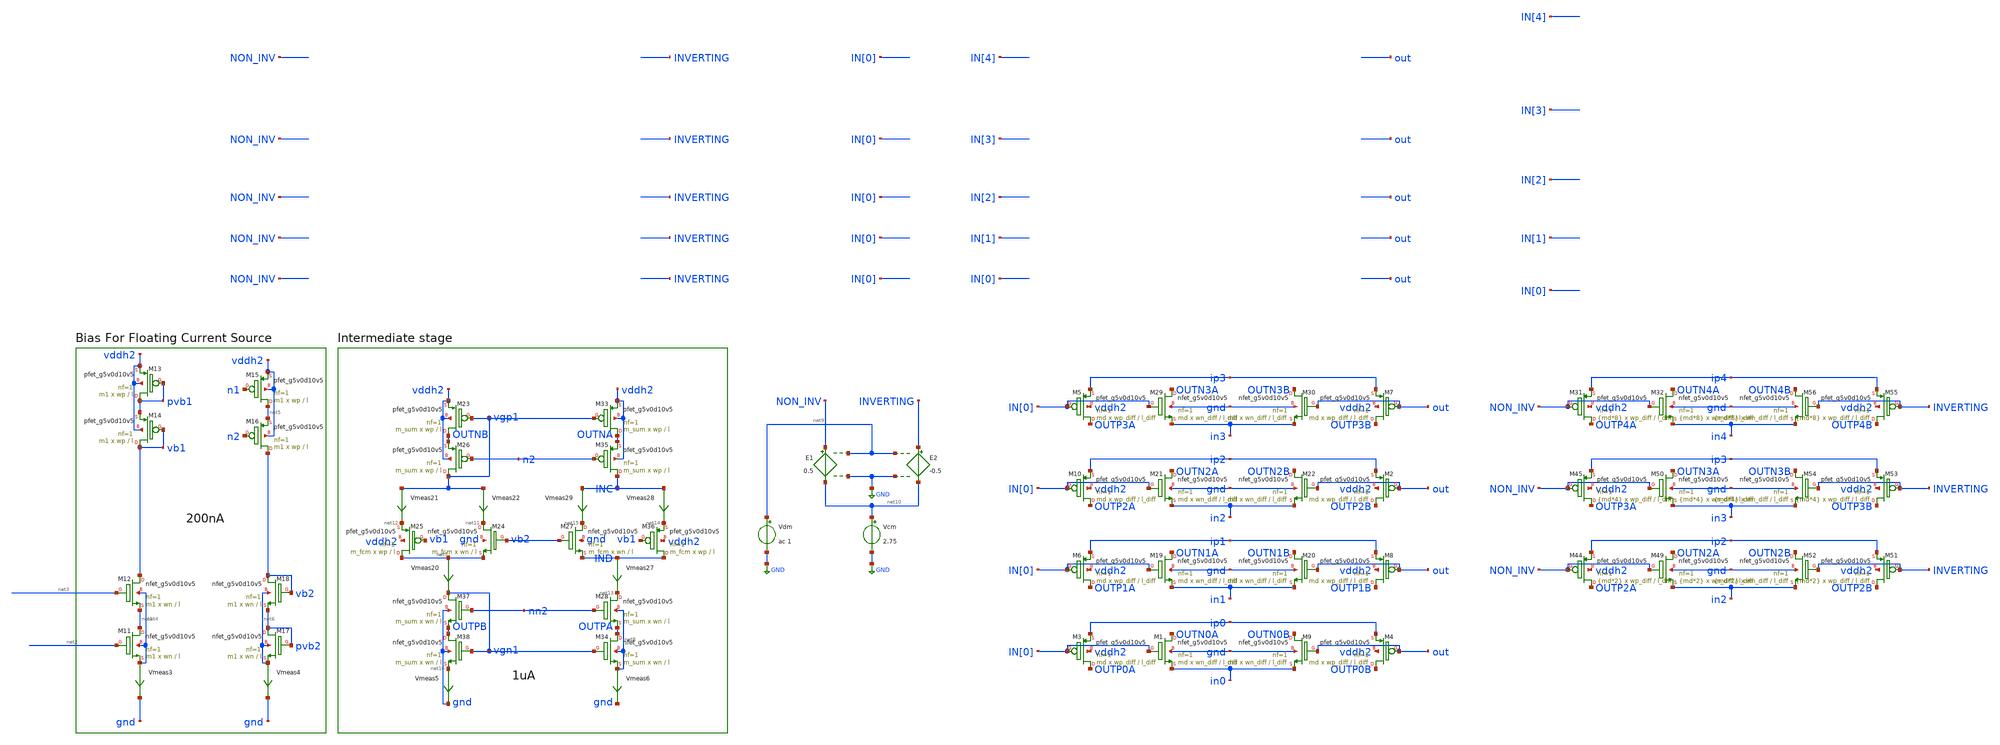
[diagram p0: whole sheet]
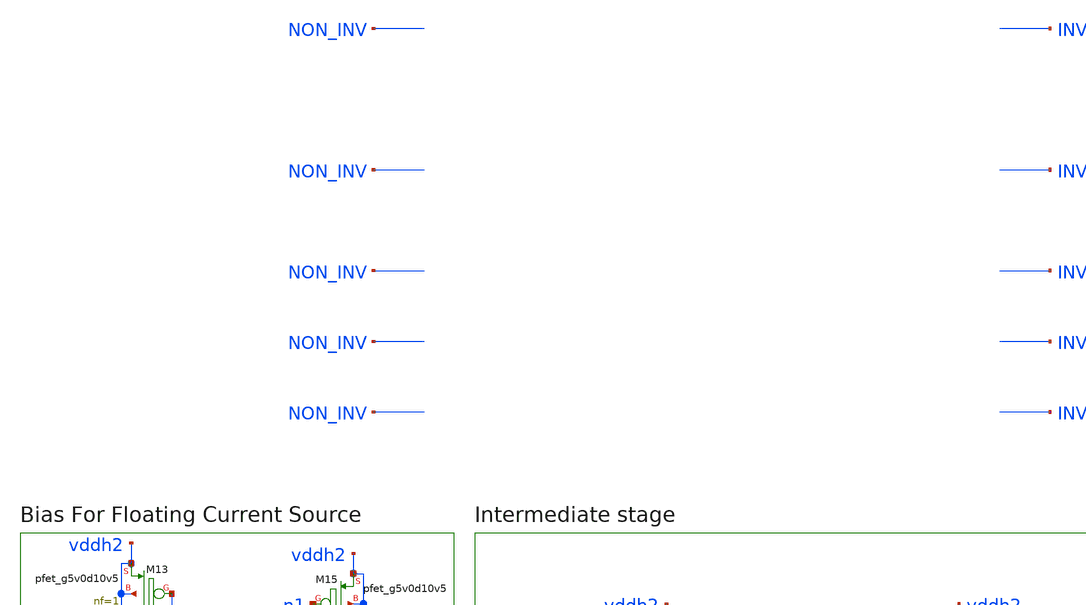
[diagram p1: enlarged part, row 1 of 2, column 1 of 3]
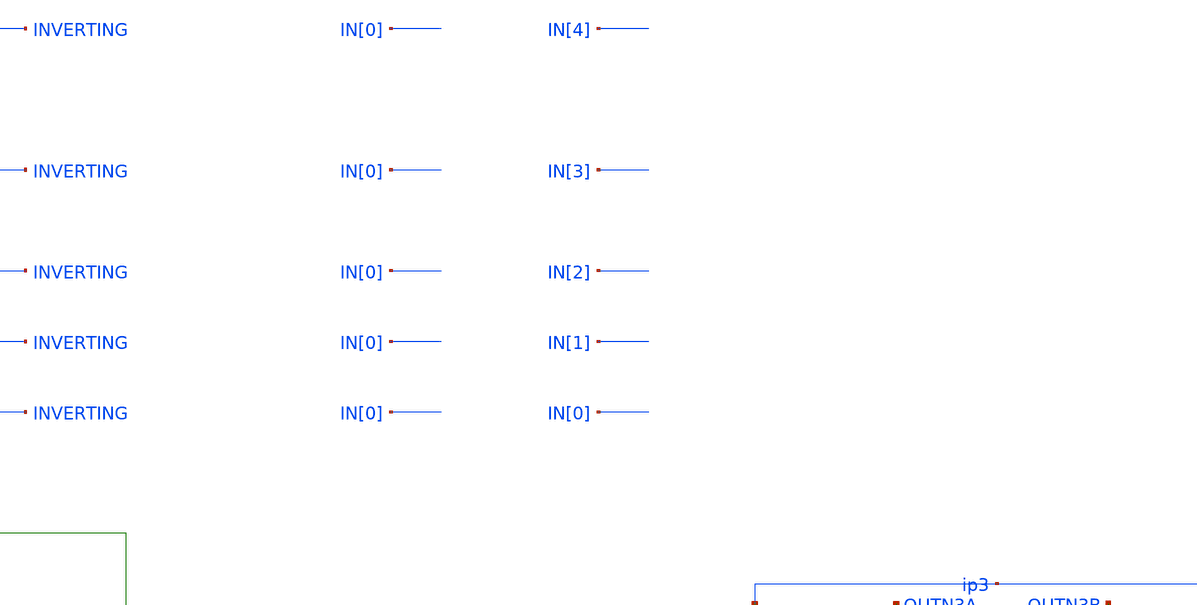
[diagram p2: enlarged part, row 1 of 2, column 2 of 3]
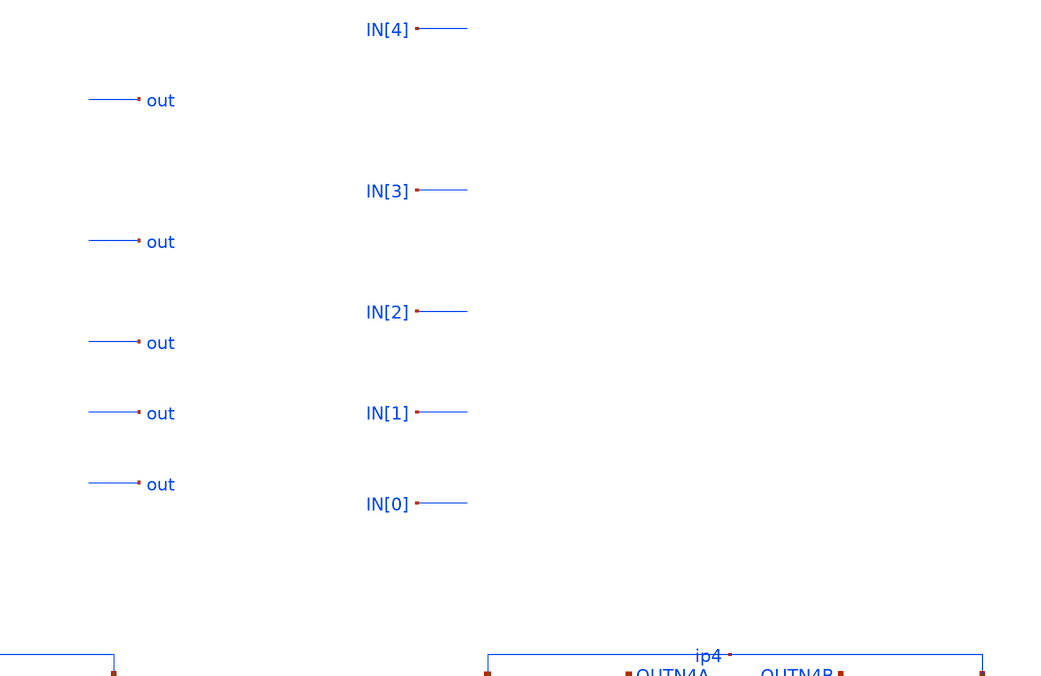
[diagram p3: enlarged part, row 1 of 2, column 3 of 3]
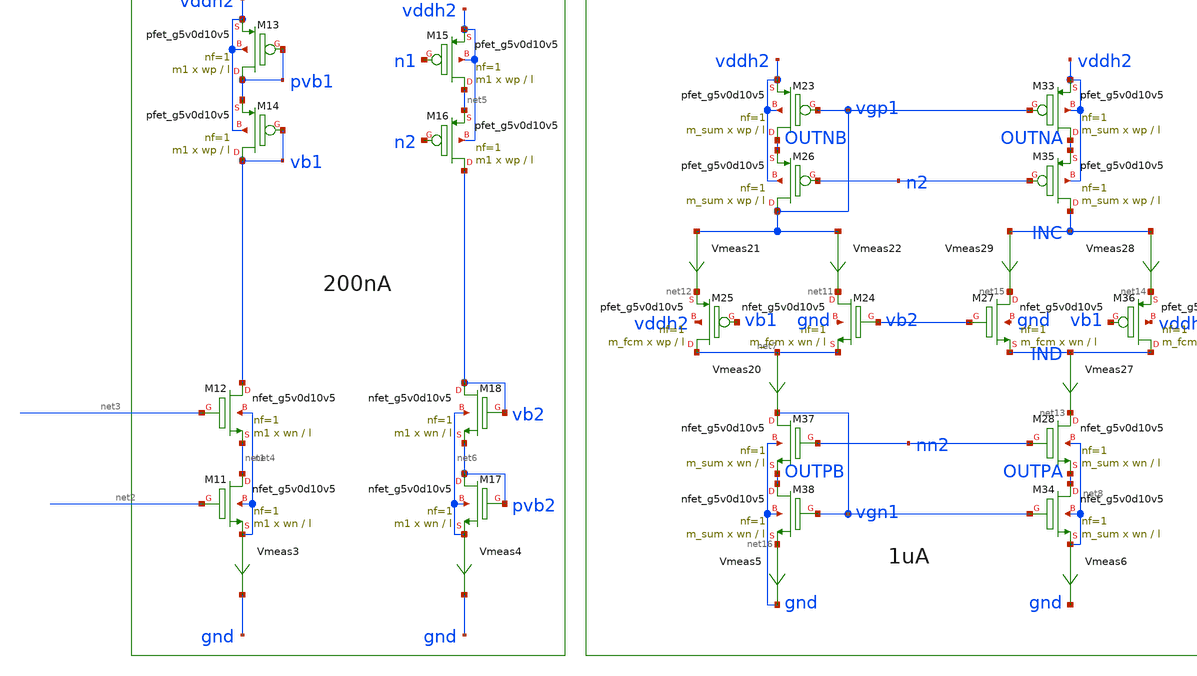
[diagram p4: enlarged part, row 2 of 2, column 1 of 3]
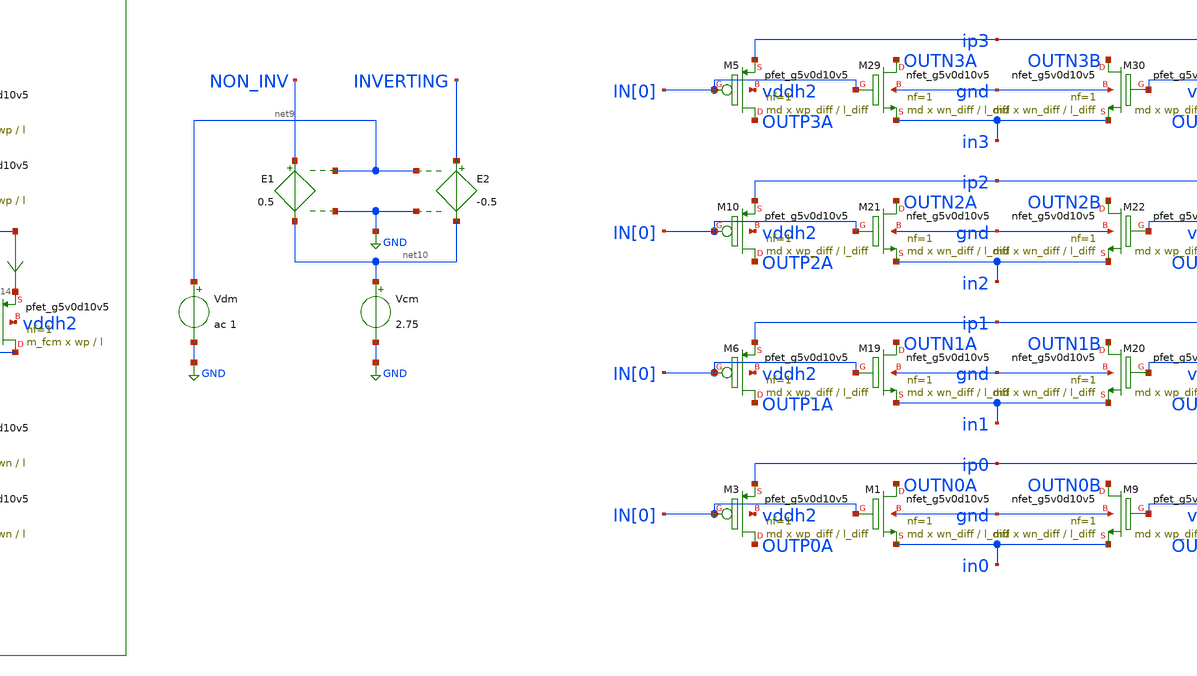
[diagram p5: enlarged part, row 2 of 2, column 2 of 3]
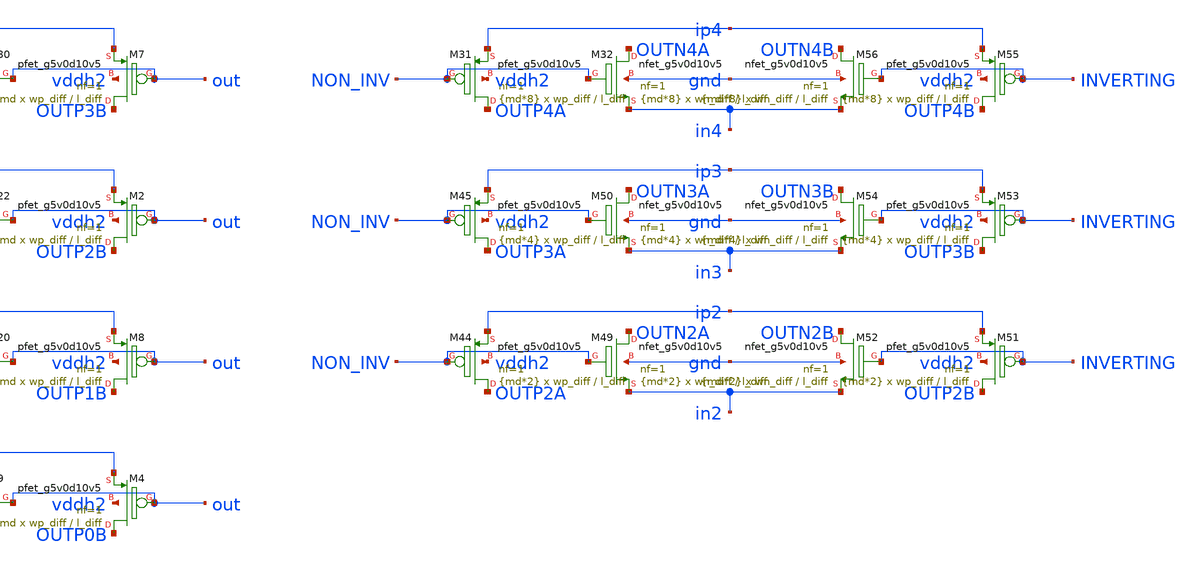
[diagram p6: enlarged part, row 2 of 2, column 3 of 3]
** sch_path: xschem/untitled-1.sch
**.subckt untitled-1
XM11 net1 net2 net4 net4 sky130_fd_pr__nfet_g5v0d10v5 L=l W=wn nf=1 ad='int((nf+1)/2) * W/nf * 0.29'
+ as='int((nf+2)/2) * W/nf * 0.29' pd='2*int((nf+1)/2) * (W/nf + 0.29)' ps='2*int((nf+2)/2) * (W/nf + 0.29)'
+ nrd='0.29 / W' nrs='0.29 / W' sa=0 sb=0 sd=0 mult=m1 m=m1
XM12 vb1 net3 net1 net4 sky130_fd_pr__nfet_g5v0d10v5 L=l W=wn nf=1 ad='int((nf+1)/2) * W/nf * 0.29' as='int((nf+2)/2) * W/nf * 0.29'
+ pd='2*int((nf+1)/2) * (W/nf + 0.29)' ps='2*int((nf+2)/2) * (W/nf + 0.29)' nrd='0.29 / W' nrs='0.29 / W'
+ sa=0 sb=0 sd=0 mult=m1 m=m1
Vmeas3 net4 gnd 0
.save i(vmeas3)
XM17 pvb2 pvb2 net6 net6 sky130_fd_pr__nfet_g5v0d10v5 L=l W=wn nf=1 ad='int((nf+1)/2) * W/nf * 0.29'
+ as='int((nf+2)/2) * W/nf * 0.29' pd='2*int((nf+1)/2) * (W/nf + 0.29)' ps='2*int((nf+2)/2) * (W/nf + 0.29)'
+ nrd='0.29 / W' nrs='0.29 / W' sa=0 sb=0 sd=0 mult=m1 m=m1
XM18 vb2 vb2 pvb2 net6 sky130_fd_pr__nfet_g5v0d10v5 L=l W=wn nf=1 ad='int((nf+1)/2) * W/nf * 0.29' as='int((nf+2)/2) * W/nf * 0.29'
+ pd='2*int((nf+1)/2) * (W/nf + 0.29)' ps='2*int((nf+2)/2) * (W/nf + 0.29)' nrd='0.29 / W' nrs='0.29 / W'
+ sa=0 sb=0 sd=0 mult=m1 m=m1
Vmeas4 net6 gnd 0
.save i(vmeas4)
Vmeas20 net7 vgn1 0
.save i(vmeas20)
XM23 OUTNB vgp1 vddh2 vddh2 sky130_fd_pr__pfet_g5v0d10v5 L=l W=wp nf=1 ad='int((nf+1)/2) * W/nf * 0.29'
+ as='int((nf+2)/2) * W/nf * 0.29' pd='2*int((nf+1)/2) * (W/nf + 0.29)' ps='2*int((nf+2)/2) * (W/nf + 0.29)'
+ nrd='0.29 / W' nrs='0.29 / W' sa=0 sb=0 sd=0 mult=m_sum m=m_sum
XM24 net11 vb2 net7 gnd sky130_fd_pr__nfet_g5v0d10v5 L=l W=wn nf=1 ad='int((nf+1)/2) * W/nf * 0.29' as='int((nf+2)/2) * W/nf * 0.29'
+ pd='2*int((nf+1)/2) * (W/nf + 0.29)' ps='2*int((nf+2)/2) * (W/nf + 0.29)' nrd='0.29 / W' nrs='0.29 / W'
+ sa=0 sb=0 sd=0 mult=m_fcm m=m_fcm
Vmeas21 vgp1 net12 0
.save i(vmeas21)
Vmeas22 vgp1 net11 0
.save i(vmeas22)
XM25 net7 vb1 net12 vddh2 sky130_fd_pr__pfet_g5v0d10v5 L=l W=wp nf=1 ad='int((nf+1)/2) * W/nf * 0.29'
+ as='int((nf+2)/2) * W/nf * 0.29' pd='2*int((nf+1)/2) * (W/nf + 0.29)' ps='2*int((nf+2)/2) * (W/nf + 0.29)'
+ nrd='0.29 / W' nrs='0.29 / W' sa=0 sb=0 sd=0 mult=m_fcm m=m_fcm
Vmeas27 IND net13 0
.save i(vmeas27)
Vmeas28 INC net14 0
.save i(vmeas28)
Vmeas29 INC net15 0
.save i(vmeas29)
XM26 vgp1 n2 OUTNB vddh2 sky130_fd_pr__pfet_g5v0d10v5 L=l W=wp nf=1 ad='int((nf+1)/2) * W/nf * 0.29'
+ as='int((nf+2)/2) * W/nf * 0.29' pd='2*int((nf+1)/2) * (W/nf + 0.29)' ps='2*int((nf+2)/2) * (W/nf + 0.29)'
+ nrd='0.29 / W' nrs='0.29 / W' sa=0 sb=0 sd=0 mult=m_sum m=m_sum
XM33 OUTNA vgp1 vddh2 vddh2 sky130_fd_pr__pfet_g5v0d10v5 L=l W=wp nf=1 ad='int((nf+1)/2) * W/nf * 0.29'
+ as='int((nf+2)/2) * W/nf * 0.29' pd='2*int((nf+1)/2) * (W/nf + 0.29)' ps='2*int((nf+2)/2) * (W/nf + 0.29)'
+ nrd='0.29 / W' nrs='0.29 / W' sa=0 sb=0 sd=0 mult=m_sum m=m_sum
XM35 INC n2 OUTNA vddh2 sky130_fd_pr__pfet_g5v0d10v5 L=l W=wp nf=1 ad='int((nf+1)/2) * W/nf * 0.29' as='int((nf+2)/2) * W/nf * 0.29'
+ pd='2*int((nf+1)/2) * (W/nf + 0.29)' ps='2*int((nf+2)/2) * (W/nf + 0.29)' nrd='0.29 / W' nrs='0.29 / W'
+ sa=0 sb=0 sd=0 mult=m_sum m=m_sum
XM28 net13 nn2 OUTPA net8 sky130_fd_pr__nfet_g5v0d10v5 L=l W=wn nf=1 ad='int((nf+1)/2) * W/nf * 0.29'
+ as='int((nf+2)/2) * W/nf * 0.29' pd='2*int((nf+1)/2) * (W/nf + 0.29)' ps='2*int((nf+2)/2) * (W/nf + 0.29)'
+ nrd='0.29 / W' nrs='0.29 / W' sa=0 sb=0 sd=0 mult=m_sum m=m_sum
XM34 OUTPA vgn1 net8 net8 sky130_fd_pr__nfet_g5v0d10v5 L=l W=wn nf=1 ad='int((nf+1)/2) * W/nf * 0.29'
+ as='int((nf+2)/2) * W/nf * 0.29' pd='2*int((nf+1)/2) * (W/nf + 0.29)' ps='2*int((nf+2)/2) * (W/nf + 0.29)'
+ nrd='0.29 / W' nrs='0.29 / W' sa=0 sb=0 sd=0 mult=m_sum m=m_sum
XM37 vgn1 nn2 OUTPB gnd sky130_fd_pr__nfet_g5v0d10v5 L=l W=wn nf=1 ad='int((nf+1)/2) * W/nf * 0.29' as='int((nf+2)/2) * W/nf * 0.29'
+ pd='2*int((nf+1)/2) * (W/nf + 0.29)' ps='2*int((nf+2)/2) * (W/nf + 0.29)' nrd='0.29 / W' nrs='0.29 / W'
+ sa=0 sb=0 sd=0 mult=m_sum m=m_sum
XM38 OUTPB vgn1 net16 gnd sky130_fd_pr__nfet_g5v0d10v5 L=l W=wn nf=1 ad='int((nf+1)/2) * W/nf * 0.29'
+ as='int((nf+2)/2) * W/nf * 0.29' pd='2*int((nf+1)/2) * (W/nf + 0.29)' ps='2*int((nf+2)/2) * (W/nf + 0.29)'
+ nrd='0.29 / W' nrs='0.29 / W' sa=0 sb=0 sd=0 mult=m_sum m=m_sum
XM36 IND vb1 net14 vddh2 sky130_fd_pr__pfet_g5v0d10v5 L=l W=wp nf=1 ad='int((nf+1)/2) * W/nf * 0.29'
+ as='int((nf+2)/2) * W/nf * 0.29' pd='2*int((nf+1)/2) * (W/nf + 0.29)' ps='2*int((nf+2)/2) * (W/nf + 0.29)'
+ nrd='0.29 / W' nrs='0.29 / W' sa=0 sb=0 sd=0 mult=m_fcm m=m_fcm
XM27 net15 vb2 IND gnd sky130_fd_pr__nfet_g5v0d10v5 L=l W=wn nf=1 ad='int((nf+1)/2) * W/nf * 0.29' as='int((nf+2)/2) * W/nf * 0.29'
+ pd='2*int((nf+1)/2) * (W/nf + 0.29)' ps='2*int((nf+2)/2) * (W/nf + 0.29)' nrd='0.29 / W' nrs='0.29 / W'
+ sa=0 sb=0 sd=0 mult=m_fcm m=m_fcm
XM13 pvb1 pvb1 vddh2 vddh2 sky130_fd_pr__pfet_g5v0d10v5 L=l W=wp nf=1 ad='int((nf+1)/2) * W/nf * 0.29'
+ as='int((nf+2)/2) * W/nf * 0.29' pd='2*int((nf+1)/2) * (W/nf + 0.29)' ps='2*int((nf+2)/2) * (W/nf + 0.29)'
+ nrd='0.29 / W' nrs='0.29 / W' sa=0 sb=0 sd=0 mult=m1 m=m1
XM14 vb1 vb1 pvb1 vddh2 sky130_fd_pr__pfet_g5v0d10v5 L=l W=wp nf=1 ad='int((nf+1)/2) * W/nf * 0.29' as='int((nf+2)/2) * W/nf * 0.29'
+ pd='2*int((nf+1)/2) * (W/nf + 0.29)' ps='2*int((nf+2)/2) * (W/nf + 0.29)' nrd='0.29 / W' nrs='0.29 / W'
+ sa=0 sb=0 sd=0 mult=m1 m=m1
XM15 net5 n1 vddh2 vddh2 sky130_fd_pr__pfet_g5v0d10v5 L=l W=wp nf=1 ad='int((nf+1)/2) * W/nf * 0.29'
+ as='int((nf+2)/2) * W/nf * 0.29' pd='2*int((nf+1)/2) * (W/nf + 0.29)' ps='2*int((nf+2)/2) * (W/nf + 0.29)'
+ nrd='0.29 / W' nrs='0.29 / W' sa=0 sb=0 sd=0 mult=m1 m=m1
XM16 vb2 n2 net5 vddh2 sky130_fd_pr__pfet_g5v0d10v5 L=l W=wp nf=1 ad='int((nf+1)/2) * W/nf * 0.29' as='int((nf+2)/2) * W/nf * 0.29'
+ pd='2*int((nf+1)/2) * (W/nf + 0.29)' ps='2*int((nf+2)/2) * (W/nf + 0.29)' nrd='0.29 / W' nrs='0.29 / W'
+ sa=0 sb=0 sd=0 mult=m1 m=m1
Vmeas5 net16 gnd 0
.save i(vmeas5)
Vmeas6 net8 gnd 0
.save i(vmeas6)
E1 NON_INV net10 net9 GND 0.5
E2 INVERTING net10 net9 GND -0.5
Vdm net9 GND ac 1
Vcm net10 GND 2.75
XM1 OUTN0A IN[0] in0 gnd sky130_fd_pr__nfet_g5v0d10v5 L=l_diff W=wn_diff nf=1 ad='int((nf+1)/2) * W/nf * 0.29'
+ as='int((nf+2)/2) * W/nf * 0.29' pd='2*int((nf+1)/2) * (W/nf + 0.29)' ps='2*int((nf+2)/2) * (W/nf + 0.29)'
+ nrd='0.29 / W' nrs='0.29 / W' sa=0 sb=0 sd=0 mult=md m=md
XM3 OUTP0A IN[0] ip0 vddh2 sky130_fd_pr__pfet_g5v0d10v5 L=l_diff W=wp_diff nf=1 ad='int((nf+1)/2) * W/nf * 0.29'
+ as='int((nf+2)/2) * W/nf * 0.29' pd='2*int((nf+1)/2) * (W/nf + 0.29)' ps='2*int((nf+2)/2) * (W/nf + 0.29)'
+ nrd='0.29 / W' nrs='0.29 / W' sa=0 sb=0 sd=0 mult=md m=md
XM4 OUTP0B out ip0 vddh2 sky130_fd_pr__pfet_g5v0d10v5 L=l_diff W=wp_diff nf=1 ad='int((nf+1)/2) * W/nf * 0.29'
+ as='int((nf+2)/2) * W/nf * 0.29' pd='2*int((nf+1)/2) * (W/nf + 0.29)' ps='2*int((nf+2)/2) * (W/nf + 0.29)'
+ nrd='0.29 / W' nrs='0.29 / W' sa=0 sb=0 sd=0 mult=md m=md
XM6 OUTP1A IN[0] ip1 vddh2 sky130_fd_pr__pfet_g5v0d10v5 L=l_diff W=wp_diff nf=1 ad='int((nf+1)/2) * W/nf * 0.29'
+ as='int((nf+2)/2) * W/nf * 0.29' pd='2*int((nf+1)/2) * (W/nf + 0.29)' ps='2*int((nf+2)/2) * (W/nf + 0.29)'
+ nrd='0.29 / W' nrs='0.29 / W' sa=0 sb=0 sd=0 mult=md m=md
XM8 OUTP1B out ip1 vddh2 sky130_fd_pr__pfet_g5v0d10v5 L=l_diff W=wp_diff nf=1 ad='int((nf+1)/2) * W/nf * 0.29'
+ as='int((nf+2)/2) * W/nf * 0.29' pd='2*int((nf+1)/2) * (W/nf + 0.29)' ps='2*int((nf+2)/2) * (W/nf + 0.29)'
+ nrd='0.29 / W' nrs='0.29 / W' sa=0 sb=0 sd=0 mult=md m=md
XM10 OUTP2A IN[0] ip2 vddh2 sky130_fd_pr__pfet_g5v0d10v5 L=l_diff W=wp_diff nf=1 ad='int((nf+1)/2) * W/nf * 0.29'
+ as='int((nf+2)/2) * W/nf * 0.29' pd='2*int((nf+1)/2) * (W/nf + 0.29)' ps='2*int((nf+2)/2) * (W/nf + 0.29)'
+ nrd='0.29 / W' nrs='0.29 / W' sa=0 sb=0 sd=0 mult=md m=md
XM2 OUTP2B out ip2 vddh2 sky130_fd_pr__pfet_g5v0d10v5 L=l_diff W=wp_diff nf=1 ad='int((nf+1)/2) * W/nf * 0.29'
+ as='int((nf+2)/2) * W/nf * 0.29' pd='2*int((nf+1)/2) * (W/nf + 0.29)' ps='2*int((nf+2)/2) * (W/nf + 0.29)'
+ nrd='0.29 / W' nrs='0.29 / W' sa=0 sb=0 sd=0 mult=md m=md
XM5 OUTP3A IN[0] ip3 vddh2 sky130_fd_pr__pfet_g5v0d10v5 L=l_diff W=wp_diff nf=1 ad='int((nf+1)/2) * W/nf * 0.29'
+ as='int((nf+2)/2) * W/nf * 0.29' pd='2*int((nf+1)/2) * (W/nf + 0.29)' ps='2*int((nf+2)/2) * (W/nf + 0.29)'
+ nrd='0.29 / W' nrs='0.29 / W' sa=0 sb=0 sd=0 mult=md m=md
XM7 OUTP3B out ip3 vddh2 sky130_fd_pr__pfet_g5v0d10v5 L=l_diff W=wp_diff nf=1 ad='int((nf+1)/2) * W/nf * 0.29'
+ as='int((nf+2)/2) * W/nf * 0.29' pd='2*int((nf+1)/2) * (W/nf + 0.29)' ps='2*int((nf+2)/2) * (W/nf + 0.29)'
+ nrd='0.29 / W' nrs='0.29 / W' sa=0 sb=0 sd=0 mult=md m=md
XM9 OUTN0B out in0 gnd sky130_fd_pr__nfet_g5v0d10v5 L=l_diff W=wn_diff nf=1 ad='int((nf+1)/2) * W/nf * 0.29'
+ as='int((nf+2)/2) * W/nf * 0.29' pd='2*int((nf+1)/2) * (W/nf + 0.29)' ps='2*int((nf+2)/2) * (W/nf + 0.29)'
+ nrd='0.29 / W' nrs='0.29 / W' sa=0 sb=0 sd=0 mult=md m=md
XM19 OUTN1A IN[0] in1 gnd sky130_fd_pr__nfet_g5v0d10v5 L=l_diff W=wn_diff nf=1 ad='int((nf+1)/2) * W/nf * 0.29'
+ as='int((nf+2)/2) * W/nf * 0.29' pd='2*int((nf+1)/2) * (W/nf + 0.29)' ps='2*int((nf+2)/2) * (W/nf + 0.29)'
+ nrd='0.29 / W' nrs='0.29 / W' sa=0 sb=0 sd=0 mult=md m=md
XM20 OUTN1B out in1 gnd sky130_fd_pr__nfet_g5v0d10v5 L=l_diff W=wn_diff nf=1 ad='int((nf+1)/2) * W/nf * 0.29'
+ as='int((nf+2)/2) * W/nf * 0.29' pd='2*int((nf+1)/2) * (W/nf + 0.29)' ps='2*int((nf+2)/2) * (W/nf + 0.29)'
+ nrd='0.29 / W' nrs='0.29 / W' sa=0 sb=0 sd=0 mult=md m=md
XM21 OUTN2A IN[0] in2 gnd sky130_fd_pr__nfet_g5v0d10v5 L=l_diff W=wn_diff nf=1 ad='int((nf+1)/2) * W/nf * 0.29'
+ as='int((nf+2)/2) * W/nf * 0.29' pd='2*int((nf+1)/2) * (W/nf + 0.29)' ps='2*int((nf+2)/2) * (W/nf + 0.29)'
+ nrd='0.29 / W' nrs='0.29 / W' sa=0 sb=0 sd=0 mult=md m=md
XM22 OUTN2B out in2 gnd sky130_fd_pr__nfet_g5v0d10v5 L=l_diff W=wn_diff nf=1 ad='int((nf+1)/2) * W/nf * 0.29'
+ as='int((nf+2)/2) * W/nf * 0.29' pd='2*int((nf+1)/2) * (W/nf + 0.29)' ps='2*int((nf+2)/2) * (W/nf + 0.29)'
+ nrd='0.29 / W' nrs='0.29 / W' sa=0 sb=0 sd=0 mult=md m=md
XM29 OUTN3A IN[0] in3 gnd sky130_fd_pr__nfet_g5v0d10v5 L=l_diff W=wn_diff nf=1 ad='int((nf+1)/2) * W/nf * 0.29'
+ as='int((nf+2)/2) * W/nf * 0.29' pd='2*int((nf+1)/2) * (W/nf + 0.29)' ps='2*int((nf+2)/2) * (W/nf + 0.29)'
+ nrd='0.29 / W' nrs='0.29 / W' sa=0 sb=0 sd=0 mult=md m=md
XM30 OUTN3B out in3 gnd sky130_fd_pr__nfet_g5v0d10v5 L=l_diff W=wn_diff nf=1 ad='int((nf+1)/2) * W/nf * 0.29'
+ as='int((nf+2)/2) * W/nf * 0.29' pd='2*int((nf+1)/2) * (W/nf + 0.29)' ps='2*int((nf+2)/2) * (W/nf + 0.29)'
+ nrd='0.29 / W' nrs='0.29 / W' sa=0 sb=0 sd=0 mult=md m=md
XM31 OUTP4A NON_INV ip4 vddh2 sky130_fd_pr__pfet_g5v0d10v5 L=l_diff W=wp_diff nf=1 ad='int((nf+1)/2) * W/nf * 0.29'
+ as='int((nf+2)/2) * W/nf * 0.29' pd='2*int((nf+1)/2) * (W/nf + 0.29)' ps='2*int((nf+2)/2) * (W/nf + 0.29)'
+ nrd='0.29 / W' nrs='0.29 / W' sa=0 sb=0 sd=0 mult={md*8} m={md*8}
XM32 OUTN4A NON_INV in4 gnd sky130_fd_pr__nfet_g5v0d10v5 L=l_diff W=wn_diff nf=1 ad='int((nf+1)/2) * W/nf * 0.29'
+ as='int((nf+2)/2) * W/nf * 0.29' pd='2*int((nf+1)/2) * (W/nf + 0.29)' ps='2*int((nf+2)/2) * (W/nf + 0.29)'
+ nrd='0.29 / W' nrs='0.29 / W' sa=0 sb=0 sd=0 mult={md*8} m={md*8}
XM44 OUTP2A NON_INV ip2 vddh2 sky130_fd_pr__pfet_g5v0d10v5 L=l_diff W=wp_diff nf=1 ad='int((nf+1)/2) * W/nf * 0.29'
+ as='int((nf+2)/2) * W/nf * 0.29' pd='2*int((nf+1)/2) * (W/nf + 0.29)' ps='2*int((nf+2)/2) * (W/nf + 0.29)'
+ nrd='0.29 / W' nrs='0.29 / W' sa=0 sb=0 sd=0 mult={md*2} m={md*2}
XM45 OUTP3A NON_INV ip3 vddh2 sky130_fd_pr__pfet_g5v0d10v5 L=l_diff W=wp_diff nf=1 ad='int((nf+1)/2) * W/nf * 0.29'
+ as='int((nf+2)/2) * W/nf * 0.29' pd='2*int((nf+1)/2) * (W/nf + 0.29)' ps='2*int((nf+2)/2) * (W/nf + 0.29)'
+ nrd='0.29 / W' nrs='0.29 / W' sa=0 sb=0 sd=0 mult={md*4} m={md*4}
XM49 OUTN2A NON_INV in2 gnd sky130_fd_pr__nfet_g5v0d10v5 L=l_diff W=wn_diff nf=1 ad='int((nf+1)/2) * W/nf * 0.29'
+ as='int((nf+2)/2) * W/nf * 0.29' pd='2*int((nf+1)/2) * (W/nf + 0.29)' ps='2*int((nf+2)/2) * (W/nf + 0.29)'
+ nrd='0.29 / W' nrs='0.29 / W' sa=0 sb=0 sd=0 mult={md*2} m={md*2}
XM50 OUTN3A NON_INV in3 gnd sky130_fd_pr__nfet_g5v0d10v5 L=l_diff W=wn_diff nf=1 ad='int((nf+1)/2) * W/nf * 0.29'
+ as='int((nf+2)/2) * W/nf * 0.29' pd='2*int((nf+1)/2) * (W/nf + 0.29)' ps='2*int((nf+2)/2) * (W/nf + 0.29)'
+ nrd='0.29 / W' nrs='0.29 / W' sa=0 sb=0 sd=0 mult={md*4} m={md*4}
XM51 OUTP2B INVERTING ip2 vddh2 sky130_fd_pr__pfet_g5v0d10v5 L=l_diff W=wp_diff nf=1 ad='int((nf+1)/2) * W/nf * 0.29'
+ as='int((nf+2)/2) * W/nf * 0.29' pd='2*int((nf+1)/2) * (W/nf + 0.29)' ps='2*int((nf+2)/2) * (W/nf + 0.29)'
+ nrd='0.29 / W' nrs='0.29 / W' sa=0 sb=0 sd=0 mult={md*2} m={md*2}
XM52 OUTN2B INVERTING in2 gnd sky130_fd_pr__nfet_g5v0d10v5 L=l_diff W=wn_diff nf=1 ad='int((nf+1)/2) * W/nf * 0.29'
+ as='int((nf+2)/2) * W/nf * 0.29' pd='2*int((nf+1)/2) * (W/nf + 0.29)' ps='2*int((nf+2)/2) * (W/nf + 0.29)'
+ nrd='0.29 / W' nrs='0.29 / W' sa=0 sb=0 sd=0 mult={md*2} m={md*2}
XM53 OUTP3B INVERTING ip3 vddh2 sky130_fd_pr__pfet_g5v0d10v5 L=l_diff W=wp_diff nf=1 ad='int((nf+1)/2) * W/nf * 0.29'
+ as='int((nf+2)/2) * W/nf * 0.29' pd='2*int((nf+1)/2) * (W/nf + 0.29)' ps='2*int((nf+2)/2) * (W/nf + 0.29)'
+ nrd='0.29 / W' nrs='0.29 / W' sa=0 sb=0 sd=0 mult={md*4} m={md*4}
XM54 OUTN3B INVERTING in3 gnd sky130_fd_pr__nfet_g5v0d10v5 L=l_diff W=wn_diff nf=1 ad='int((nf+1)/2) * W/nf * 0.29'
+ as='int((nf+2)/2) * W/nf * 0.29' pd='2*int((nf+1)/2) * (W/nf + 0.29)' ps='2*int((nf+2)/2) * (W/nf + 0.29)'
+ nrd='0.29 / W' nrs='0.29 / W' sa=0 sb=0 sd=0 mult={md*4} m={md*4}
XM55 OUTP4B INVERTING ip4 vddh2 sky130_fd_pr__pfet_g5v0d10v5 L=l_diff W=wp_diff nf=1 ad='int((nf+1)/2) * W/nf * 0.29'
+ as='int((nf+2)/2) * W/nf * 0.29' pd='2*int((nf+1)/2) * (W/nf + 0.29)' ps='2*int((nf+2)/2) * (W/nf + 0.29)'
+ nrd='0.29 / W' nrs='0.29 / W' sa=0 sb=0 sd=0 mult={md*8} m={md*8}
XM56 OUTN4B INVERTING in4 gnd sky130_fd_pr__nfet_g5v0d10v5 L=l_diff W=wn_diff nf=1 ad='int((nf+1)/2) * W/nf * 0.29'
+ as='int((nf+2)/2) * W/nf * 0.29' pd='2*int((nf+1)/2) * (W/nf + 0.29)' ps='2*int((nf+2)/2) * (W/nf + 0.29)'
+ nrd='0.29 / W' nrs='0.29 / W' sa=0 sb=0 sd=0 mult={md*8} m={md*8}
**.ends
.GLOBAL GND
.end
